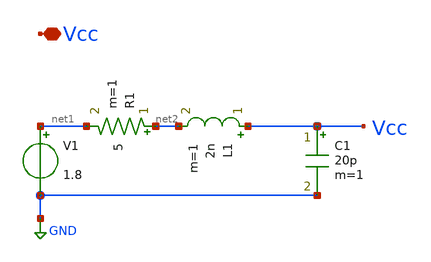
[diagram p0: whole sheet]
** sch_path: Git Files/Simulation Schematic/newVcc.sch
**.subckt newVcc Vcc
*.iopin Vcc
V1 net1 GND 1.8
R1 net2 net1 5 m=1
L1 Vcc net2 2n m=1
C1 Vcc GND 20p m=1
**.ends
.GLOBAL GND
.end
